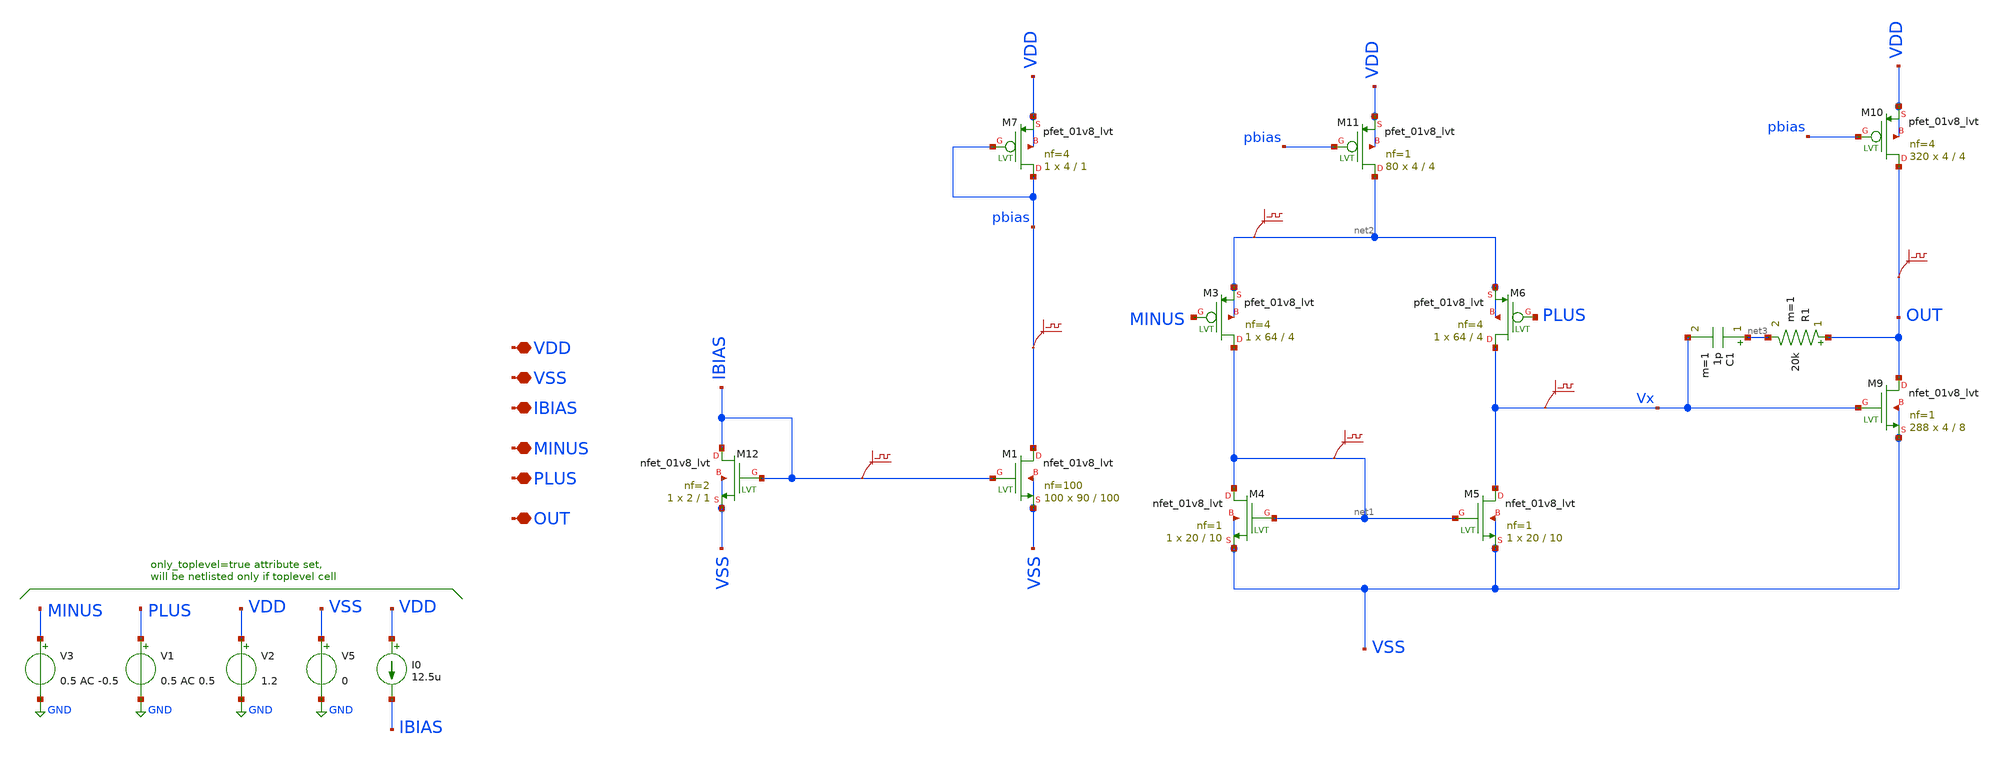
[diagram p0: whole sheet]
** sch_path: q2_opamp.sch
**.subckt q2_opamp VDD VSS MINUS PLUS OUT IBIAS
*.iopin VDD
*.iopin VSS
*.iopin MINUS
*.iopin PLUS
*.iopin OUT
*.iopin IBIAS
V1 PLUS GND 0.5 AC 0.5
V3 MINUS GND 0.5 AC -0.5
V5 VSS GND 0
I0 VDD IBIAS 12.5u
.save v(ibias)
V2 VDD GND 1.2
.save v(vx)
XM4 net1 net1 VSS VSS sky130_fd_pr__nfet_01v8_lvt L=10 W=20 nf=1 ad='int((nf+1)/2) * W/nf * 0.29' as='int((nf+2)/2) * W/nf * 0.29'
+ pd='2*int((nf+1)/2) * (W/nf + 0.29)' ps='2*int((nf+2)/2) * (W/nf + 0.29)' nrd='0.29 / W' nrs='0.29 / W'
+ sa=0 sb=0 sd=0 mult=1 m=1
XM5 Vx net1 VSS VSS sky130_fd_pr__nfet_01v8_lvt L=10 W=20 nf=1 ad='int((nf+1)/2) * W/nf * 0.29' as='int((nf+2)/2) * W/nf * 0.29'
+ pd='2*int((nf+1)/2) * (W/nf + 0.29)' ps='2*int((nf+2)/2) * (W/nf + 0.29)' nrd='0.29 / W' nrs='0.29 / W'
+ sa=0 sb=0 sd=0 mult=1 m=1
XM3 net1 MINUS net2 net2 sky130_fd_pr__pfet_01v8_lvt L=4 W=64 nf=4 ad='int((nf+1)/2) * W/nf * 0.29' as='int((nf+2)/2) * W/nf * 0.29'
+ pd='2*int((nf+1)/2) * (W/nf + 0.29)' ps='2*int((nf+2)/2) * (W/nf + 0.29)' nrd='0.29 / W' nrs='0.29 / W'
+ sa=0 sb=0 sd=0 mult=1 m=1
XM6 Vx PLUS net2 net2 sky130_fd_pr__pfet_01v8_lvt L=4 W=64 nf=4 ad='int((nf+1)/2) * W/nf * 0.29' as='int((nf+2)/2) * W/nf * 0.29'
+ pd='2*int((nf+1)/2) * (W/nf + 0.29)' ps='2*int((nf+2)/2) * (W/nf + 0.29)' nrd='0.29 / W' nrs='0.29 / W'
+ sa=0 sb=0 sd=0 mult=1 m=1
XM7 pbias pbias VDD VDD sky130_fd_pr__pfet_01v8_lvt L=1 W=4 nf=4 ad='int((nf+1)/2) * W/nf * 0.29' as='int((nf+2)/2) * W/nf * 0.29'
+ pd='2*int((nf+1)/2) * (W/nf + 0.29)' ps='2*int((nf+2)/2) * (W/nf + 0.29)' nrd='0.29 / W' nrs='0.29 / W'
+ sa=0 sb=0 sd=0 mult=1 m=1
.save v(net2)
XM9 OUT Vx VSS VSS sky130_fd_pr__nfet_01v8_lvt L=8 W=4 nf=1 ad='int((nf+1)/2) * W/nf * 0.29' as='int((nf+2)/2) * W/nf * 0.29'
+ pd='2*int((nf+1)/2) * (W/nf + 0.29)' ps='2*int((nf+2)/2) * (W/nf + 0.29)' nrd='0.29 / W' nrs='0.29 / W'
+ sa=0 sb=0 sd=0 mult=288 m=288
XM10 OUT pbias VDD VDD sky130_fd_pr__pfet_01v8_lvt L=4 W=4 nf=4 ad='int((nf+1)/2) * W/nf * 0.29' as='int((nf+2)/2) * W/nf * 0.29'
+ pd='2*int((nf+1)/2) * (W/nf + 0.29)' ps='2*int((nf+2)/2) * (W/nf + 0.29)' nrd='0.29 / W' nrs='0.29 / W'
+ sa=0 sb=0 sd=0 mult=320 m=320
XM11 net2 pbias VDD VDD sky130_fd_pr__pfet_01v8_lvt L=4 W=4 nf=1 ad='int((nf+1)/2) * W/nf * 0.29' as='int((nf+2)/2) * W/nf * 0.29'
+ pd='2*int((nf+1)/2) * (W/nf + 0.29)' ps='2*int((nf+2)/2) * (W/nf + 0.29)' nrd='0.29 / W' nrs='0.29 / W'
+ sa=0 sb=0 sd=0 mult=80 m=80
C1 net3 Vx 1p m=1
R1 OUT net3 20k m=1
.save v(net1)
.save v(out)
.save v(pbias)
XM12 IBIAS IBIAS VSS VSS sky130_fd_pr__nfet_01v8_lvt L=1 W=2 nf=2 ad='int((nf+1)/2) * W/nf * 0.29' as='int((nf+2)/2) * W/nf * 0.29'
+ pd='2*int((nf+1)/2) * (W/nf + 0.29)' ps='2*int((nf+2)/2) * (W/nf + 0.29)' nrd='0.29 / W' nrs='0.29 / W'
+ sa=0 sb=0 sd=0 mult=1 m=1
XM1 pbias IBIAS VSS VSS sky130_fd_pr__nfet_01v8_lvt L=100 W=90 nf=100 ad='int((nf+1)/2) * W/nf * 0.29'
+ as='int((nf+2)/2) * W/nf * 0.29' pd='2*int((nf+1)/2) * (W/nf + 0.29)' ps='2*int((nf+2)/2) * (W/nf + 0.29)'
+ nrd='0.29 / W' nrs='0.29 / W' sa=0 sb=0 sd=0 mult=100 m=100
**** begin user architecture code

** opencircuitdesign pdks install
.lib $::SKYWATER_MODELS/sky130.lib.spice tt





.control

ac dec 20 1 10g
run
plot db(v(out)) 180*cph(v(out))/pi
plot db(v(Vx)) 180*cph(v(Vx))/pi
reset

save @m.xm1.msky130_fd_pr__nfet_01v8[gm]
save @m.xm1.msky130_fd_pr__nfet_01v8[vth]
save @m.xm1.msky130_fd_pr__nfet_01v8[vdsat]
save @m.xm1.msky130_fd_pr__nfet_01v8[vds]
save @m.xm1.msky130_fd_pr__nfet_01v8[id]
save @m.xm1.msky130_fd_pr__nfet_01v8[gds]

save @m.xm2.msky130_fd_pr__nfet_01v8[gm]
save @m.xm2.msky130_fd_pr__nfet_01v8[vth]
save @m.xm2.msky130_fd_pr__nfet_01v8[vdsat]
save @m.xm2.msky130_fd_pr__nfet_01v8[vds]
save @m.xm2.msky130_fd_pr__nfet_01v8[id]
save @m.xm2.msky130_fd_pr__nfet_01v8[gds]

save @m.xm5.msky130_fd_pr__nfet_01v8_lvt[gm]
save @m.xm5.msky130_fd_pr__nfet_01v8_lvt[vth]
save @m.xm5.msky130_fd_pr__nfet_01v8_lvt[vdsat]
save @m.xm5.msky130_fd_pr__nfet_01v8_lvt[vds]
save @m.xm5.msky130_fd_pr__nfet_01v8_lvt[id]
save @m.xm5.msky130_fd_pr__nfet_01v8_lvt[gds]

save @m.xm6.msky130_fd_pr__pfet_01v8_lvt[gm]
save @m.xm6.msky130_fd_pr__pfet_01v8_lvt[vth]
save @m.xm6.msky130_fd_pr__pfet_01v8_lvt[vdsat]
save @m.xm6.msky130_fd_pr__pfet_01v8_lvt[vds]
save @m.xm6.msky130_fd_pr__pfet_01v8_lvt[id]
save @m.xm6.msky130_fd_pr__pfet_01v8_lvt[gds]

save @m.xm9.msky130_fd_pr__nfet_01v8_lvt[gm]
save @m.xm9.msky130_fd_pr__nfet_01v8_lvt[vth]
save @m.xm9.msky130_fd_pr__nfet_01v8_lvt[vdsat]
save @m.xm9.msky130_fd_pr__nfet_01v8_lvt[vds]
save @m.xm9.msky130_fd_pr__nfet_01v8_lvt[id]
save @m.xm9.msky130_fd_pr__nfet_01v8_lvt[gds]

save @m.xm10.msky130_fd_pr__pfet_01v8_lvt[gm]
save @m.xm10.msky130_fd_pr__pfet_01v8_lvt[vth]
save @m.xm10.msky130_fd_pr__pfet_01v8_lvt[vdsat]
save @m.xm10.msky130_fd_pr__pfet_01v8_lvt[vds]
save @m.xm10.msky130_fd_pr__pfet_01v8_lvt[id]
save @m.xm10.msky130_fd_pr__pfet_01v8_lvt[gds]

save @m.xm11.msky130_fd_pr__pfet_01v8_lvt[gm]
save @m.xm11.msky130_fd_pr__pfet_01v8_lvt[vth]
save @m.xm11.msky130_fd_pr__pfet_01v8_lvt[vdsat]
save @m.xm11.msky130_fd_pr__pfet_01v8_lvt[vds]
save @m.xm11.msky130_fd_pr__pfet_01v8_lvt[id]
save @m.xm11.msky130_fd_pr__pfet_01v8_lvt[gds]


save all
op

write q2_opamp.raw

.endc


**** end user architecture code
**.ends
.GLOBAL GND
.end
